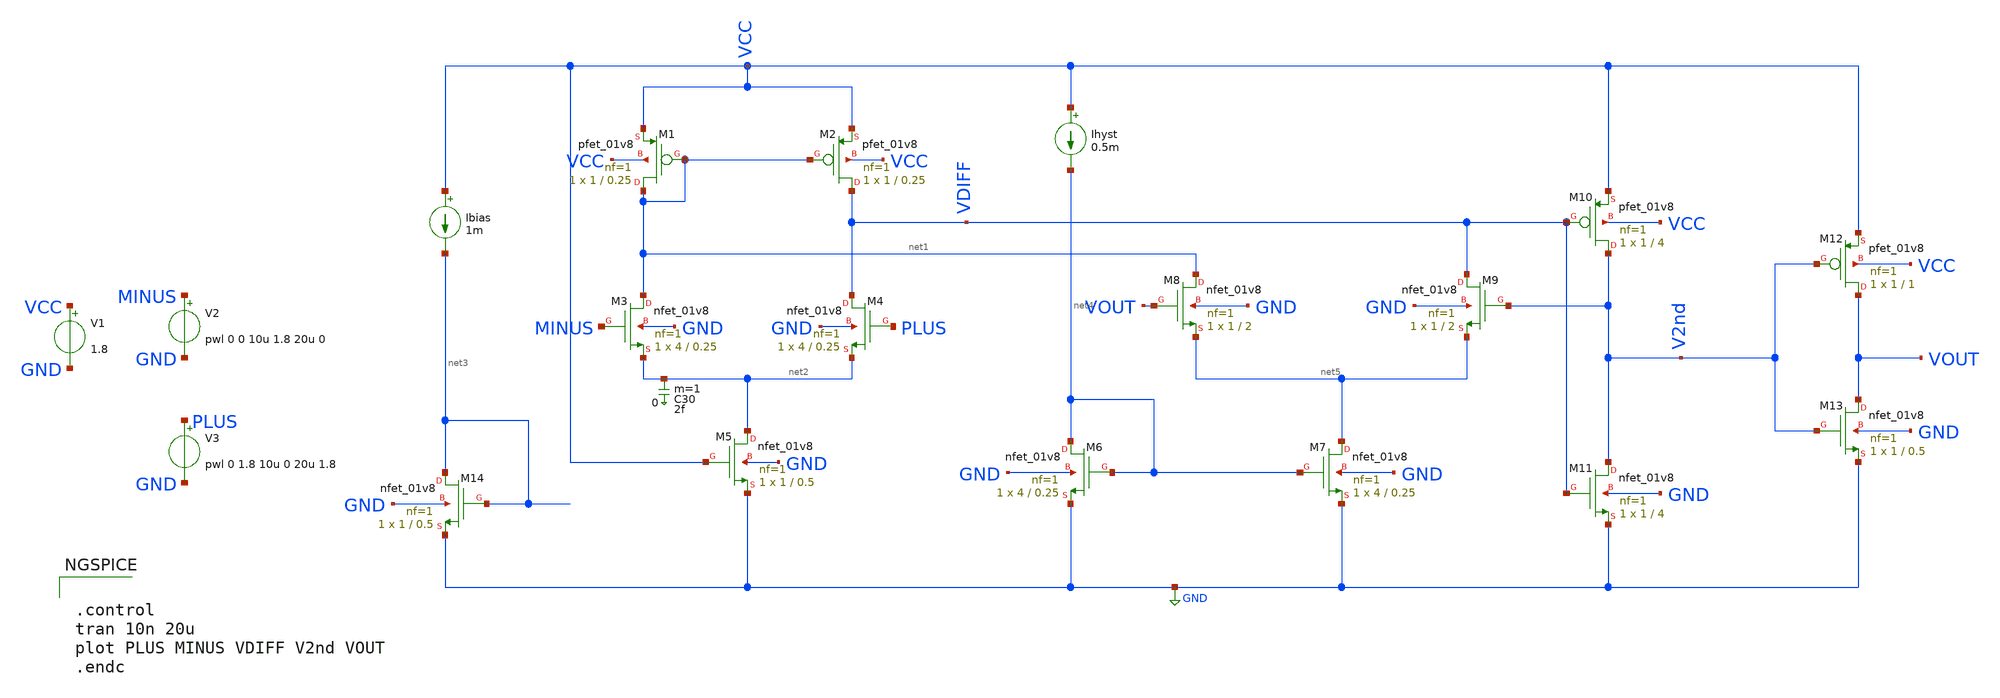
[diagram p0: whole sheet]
** sch_path: PreLayout/archive/comparator_hyst_inverter.sch
* Copyright 2020 Stefan Frederik Schippers
* Licensed under the Apache License, Version 2.0 (the "License");
* you may not use this file except in compliance with the License.
* You may obtain a copy of the License at
* https://www.apache.org/licenses/LICENSE-2.0
* Unless required by applicable law or agreed to in writing, software
* distributed under the License is distributed on an "AS IS" BASIS,
* WITHOUT WARRANTIES OR CONDITIONS OF ANY KIND, either express or implied.
* See the License for the specific language governing permissions and
* limitations under the License.
**.subckt comparator_hyst_inverter
C30 net2 0 2f m=1
XM2 VDIFF net1 VCC VCC sky130_fd_pr__pfet_01v8 L=0.25 W=1 nf=1 ad='int((nf+1)/2) * W/nf * 0.29' as='int((nf+2)/2) * W/nf * 0.29'
+ pd='2*int((nf+1)/2) * (W/nf + 0.29)' ps='2*int((nf+2)/2) * (W/nf + 0.29)' nrd='0.29 / W' nrs='0.29 / W'
+ sa=0 sb=0 sd=0 mult=1 m=1
XM1 net1 net1 VCC VCC sky130_fd_pr__pfet_01v8 L=0.25 W=1 nf=1 ad='int((nf+1)/2) * W/nf * 0.29' as='int((nf+2)/2) * W/nf * 0.29'
+ pd='2*int((nf+1)/2) * (W/nf + 0.29)' ps='2*int((nf+2)/2) * (W/nf + 0.29)' nrd='0.29 / W' nrs='0.29 / W'
+ sa=0 sb=0 sd=0 mult=1 m=1
XM5 net2 VCC GND GND sky130_fd_pr__nfet_01v8 L=0.5 W=1 nf=1 ad='int((nf+1)/2) * W/nf * 0.29' as='int((nf+2)/2) * W/nf * 0.29'
+ pd='2*int((nf+1)/2) * (W/nf + 0.29)' ps='2*int((nf+2)/2) * (W/nf + 0.29)' nrd='0.29 / W' nrs='0.29 / W'
+ sa=0 sb=0 sd=0 mult=1 m=1
XM4 VDIFF PLUS net2 GND sky130_fd_pr__nfet_01v8 L=0.25 W=4 nf=1 ad='int((nf+1)/2) * W/nf * 0.29' as='int((nf+2)/2) * W/nf * 0.29'
+ pd='2*int((nf+1)/2) * (W/nf + 0.29)' ps='2*int((nf+2)/2) * (W/nf + 0.29)' nrd='0.29 / W' nrs='0.29 / W'
+ sa=0 sb=0 sd=0 mult=1 m=1
XM3 net1 MINUS net2 GND sky130_fd_pr__nfet_01v8 L=0.25 W=4 nf=1 ad='int((nf+1)/2) * W/nf * 0.29' as='int((nf+2)/2) * W/nf * 0.29'
+ pd='2*int((nf+1)/2) * (W/nf + 0.29)' ps='2*int((nf+2)/2) * (W/nf + 0.29)' nrd='0.29 / W' nrs='0.29 / W'
+ sa=0 sb=0 sd=0 mult=1 m=1
XM7 net5 net4 GND GND sky130_fd_pr__nfet_01v8 L=0.25 W=4 nf=1 ad='int((nf+1)/2) * W/nf * 0.29' as='int((nf+2)/2) * W/nf * 0.29'
+ pd='2*int((nf+1)/2) * (W/nf + 0.29)' ps='2*int((nf+2)/2) * (W/nf + 0.29)' nrd='0.29 / W' nrs='0.29 / W'
+ sa=0 sb=0 sd=0 mult=1 m=1
XM6 net4 net4 GND GND sky130_fd_pr__nfet_01v8 L=0.25 W=4 nf=1 ad='int((nf+1)/2) * W/nf * 0.29' as='int((nf+2)/2) * W/nf * 0.29'
+ pd='2*int((nf+1)/2) * (W/nf + 0.29)' ps='2*int((nf+2)/2) * (W/nf + 0.29)' nrd='0.29 / W' nrs='0.29 / W'
+ sa=0 sb=0 sd=0 mult=1 m=1
XM8 net1 VOUT net5 GND sky130_fd_pr__nfet_01v8 L=2 W=1 nf=1 ad='int((nf+1)/2) * W/nf * 0.29' as='int((nf+2)/2) * W/nf * 0.29'
+ pd='2*int((nf+1)/2) * (W/nf + 0.29)' ps='2*int((nf+2)/2) * (W/nf + 0.29)' nrd='0.29 / W' nrs='0.29 / W'
+ sa=0 sb=0 sd=0 mult=1 m=1
XM9 VDIFF V2nd net5 GND sky130_fd_pr__nfet_01v8 L=2 W=1 nf=1 ad='int((nf+1)/2) * W/nf * 0.29' as='int((nf+2)/2) * W/nf * 0.29'
+ pd='2*int((nf+1)/2) * (W/nf + 0.29)' ps='2*int((nf+2)/2) * (W/nf + 0.29)' nrd='0.29 / W' nrs='0.29 / W'
+ sa=0 sb=0 sd=0 mult=1 m=1
XM10 V2nd VDIFF VCC VCC sky130_fd_pr__pfet_01v8 L=4 W=1 nf=1 ad='int((nf+1)/2) * W/nf * 0.29' as='int((nf+2)/2) * W/nf * 0.29'
+ pd='2*int((nf+1)/2) * (W/nf + 0.29)' ps='2*int((nf+2)/2) * (W/nf + 0.29)' nrd='0.29 / W' nrs='0.29 / W'
+ sa=0 sb=0 sd=0 mult=1 m=1
XM11 V2nd VDIFF GND GND sky130_fd_pr__nfet_01v8 L=4 W=1 nf=1 ad='int((nf+1)/2) * W/nf * 0.29' as='int((nf+2)/2) * W/nf * 0.29'
+ pd='2*int((nf+1)/2) * (W/nf + 0.29)' ps='2*int((nf+2)/2) * (W/nf + 0.29)' nrd='0.29 / W' nrs='0.29 / W'
+ sa=0 sb=0 sd=0 mult=1 m=1
XM12 VOUT V2nd VCC VCC sky130_fd_pr__pfet_01v8 L=1 W=1 nf=1 ad='int((nf+1)/2) * W/nf * 0.29' as='int((nf+2)/2) * W/nf * 0.29'
+ pd='2*int((nf+1)/2) * (W/nf + 0.29)' ps='2*int((nf+2)/2) * (W/nf + 0.29)' nrd='0.29 / W' nrs='0.29 / W'
+ sa=0 sb=0 sd=0 mult=1 m=1
XM13 VOUT V2nd GND GND sky130_fd_pr__nfet_01v8 L=0.5 W=1 nf=1 ad='int((nf+1)/2) * W/nf * 0.29' as='int((nf+2)/2) * W/nf * 0.29'
+ pd='2*int((nf+1)/2) * (W/nf + 0.29)' ps='2*int((nf+2)/2) * (W/nf + 0.29)' nrd='0.29 / W' nrs='0.29 / W'
+ sa=0 sb=0 sd=0 mult=1 m=1
XM14 net3 net3 GND GND sky130_fd_pr__nfet_01v8 L=0.5 W=1 nf=1 ad='int((nf+1)/2) * W/nf * 0.29' as='int((nf+2)/2) * W/nf * 0.29'
+ pd='2*int((nf+1)/2) * (W/nf + 0.29)' ps='2*int((nf+2)/2) * (W/nf + 0.29)' nrd='0.29 / W' nrs='0.29 / W'
+ sa=0 sb=0 sd=0 mult=1 m=1
Ibias VCC net3 1m
Ihyst VCC net4 0.5m
V1 VCC GND 1.8
V2 MINUS GND pwl 0 0 10u 1.8 20u 0
V3 PLUS GND pwl 0 1.8 10u 0 20u 1.8
**** begin user architecture code

.include $::SKYWATER_MODELS/cells/nfet_01v8/sky130_fd_pr__nfet_01v8__tt.corner.spice
.include $::SKYWATER_MODELS/cells/nfet_01v8_lvt/sky130_fd_pr__nfet_01v8_lvt__tt.corner.spice
.include $::SKYWATER_MODELS/cells/pfet_01v8/sky130_fd_pr__pfet_01v8__tt.corner.spice
.include $::SKYWATER_MODELS/cells/nfet_03v3_nvt/sky130_fd_pr__nfet_03v3_nvt__tt.corner.spice
.include $::SKYWATER_MODELS/cells/nfet_05v0_nvt/sky130_fd_pr__nfet_05v0_nvt__tt.corner.spice
.include $::SKYWATER_MODELS/cells/esd_nfet_01v8/sky130_fd_pr__esd_nfet_01v8__tt.corner.spice
.include $::SKYWATER_MODELS/cells/pfet_01v8_lvt/sky130_fd_pr__pfet_01v8_lvt__tt.corner.spice
.include $::SKYWATER_MODELS/cells/pfet_01v8_hvt/sky130_fd_pr__pfet_01v8_hvt__tt.corner.spice
.include $::SKYWATER_MODELS/cells/esd_pfet_g5v0d10v5/sky130_fd_pr__esd_pfet_g5v0d10v5__tt.corner.spice
.include $::SKYWATER_MODELS/cells/pfet_g5v0d10v5/sky130_fd_pr__pfet_g5v0d10v5__tt.corner.spice
.include $::SKYWATER_MODELS/cells/pfet_g5v0d16v0/sky130_fd_pr__pfet_g5v0d16v0__tt.corner.spice
.include $::SKYWATER_MODELS/cells/nfet_g5v0d10v5/sky130_fd_pr__nfet_g5v0d10v5__tt.corner.spice
.include $::SKYWATER_MODELS/cells/nfet_g5v0d16v0/sky130_fd_pr__nfet_g5v0d16v0__tt_discrete.corner.spice
.include $::SKYWATER_MODELS/cells/esd_nfet_g5v0d10v5/sky130_fd_pr__esd_nfet_g5v0d10v5__tt.corner.spice
.include $::SKYWATER_MODELS/models/corners/tt/nonfet.spice
* Mismatch parameters
.include $::SKYWATER_MODELS/cells/nfet_01v8/sky130_fd_pr__nfet_01v8__mismatch.corner.spice
.include $::SKYWATER_MODELS/cells/pfet_01v8/sky130_fd_pr__pfet_01v8__mismatch.corner.spice
.include $::SKYWATER_MODELS/cells/nfet_01v8_lvt/sky130_fd_pr__nfet_01v8_lvt__mismatch.corner.spice
.include $::SKYWATER_MODELS/cells/pfet_01v8_lvt/sky130_fd_pr__pfet_01v8_lvt__mismatch.corner.spice
.include $::SKYWATER_MODELS/cells/pfet_01v8_hvt/sky130_fd_pr__pfet_01v8_hvt__mismatch.corner.spice
.include $::SKYWATER_MODELS/cells/nfet_g5v0d10v5/sky130_fd_pr__nfet_g5v0d10v5__mismatch.corner.spice
.include $::SKYWATER_MODELS/cells/pfet_g5v0d10v5/sky130_fd_pr__pfet_g5v0d10v5__mismatch.corner.spice
.include $::SKYWATER_MODELS/cells/nfet_05v0_nvt/sky130_fd_pr__nfet_05v0_nvt__mismatch.corner.spice
.include $::SKYWATER_MODELS/cells/nfet_03v3_nvt/sky130_fd_pr__nfet_03v3_nvt__mismatch.corner.spice
* Resistor$::SKYWATER_MODELS/Capacitor
.include $::SKYWATER_MODELS/models/r+c/res_typical__cap_typical.spice
.include $::SKYWATER_MODELS/models/r+c/res_typical__cap_typical__lin.spice
* Special cells
.include $::SKYWATER_MODELS/models/corners/tt/specialized_cells.spice
* All models
.include $::SKYWATER_MODELS/models/all.spice
* Corner
.include $::SKYWATER_MODELS/models/corners/tt/rf.spice



.control
tran 10n 20u
plot PLUS MINUS VDIFF V2nd VOUT
.endc


**** end user architecture code
**.ends
.GLOBAL GND
.end
